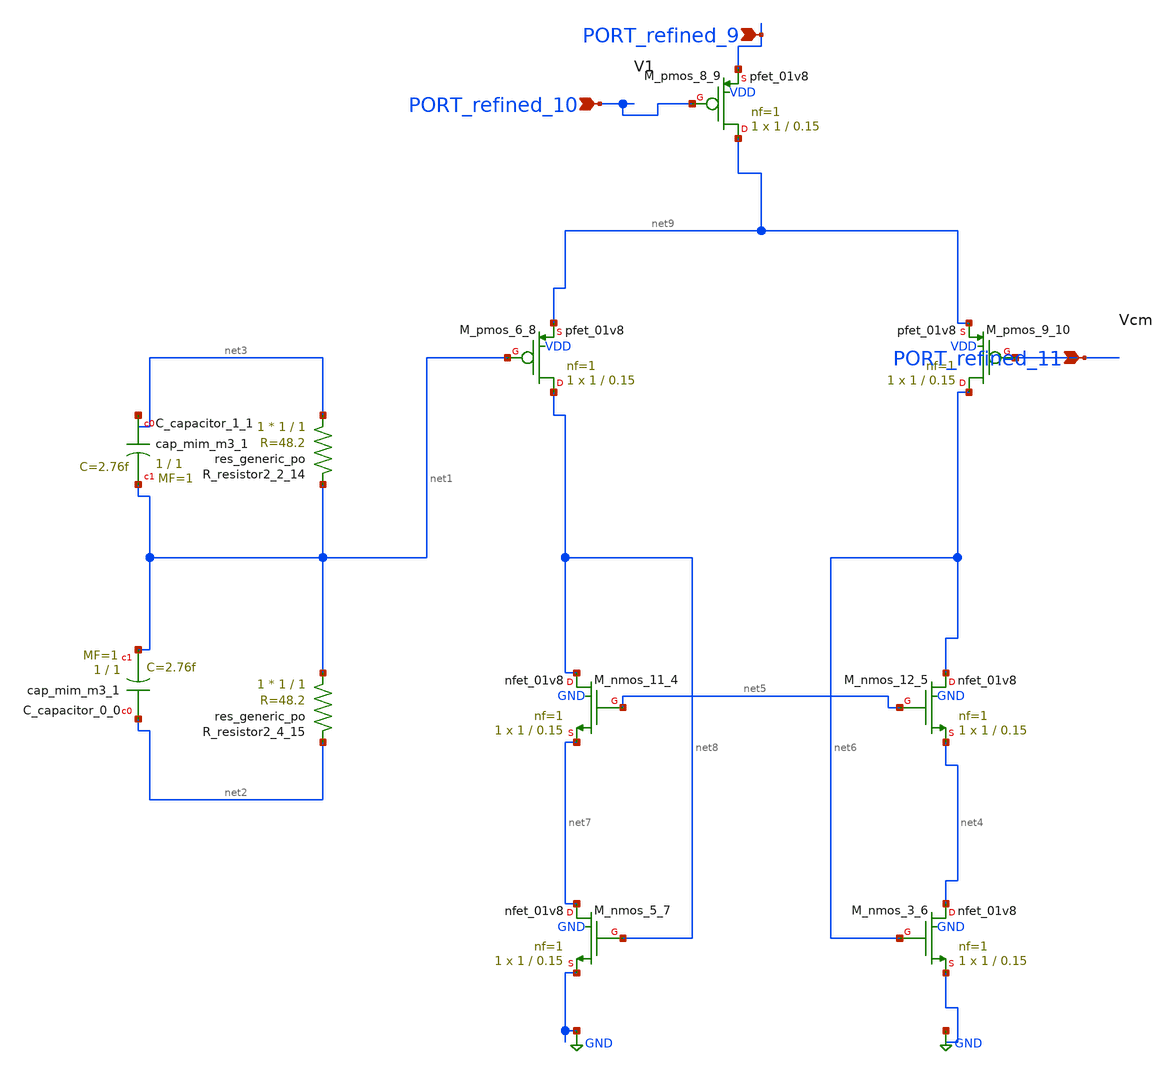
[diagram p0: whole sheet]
** sch_path: schematics/p07_fig9_cmfb.sch
**.subckt p07_fig9_cmfb PORT_refined_9 PORT_refined_10 PORT_refined_11
*.ipin PORT_refined_9
*.ipin PORT_refined_10
*.ipin PORT_refined_11
XC_capacitor_0_0 net2 net1 sky130_fd_pr__cap_mim_m3_1 W=1 L=1 MF=1 m=1
XC_capacitor_1_1 net3 net1 sky130_fd_pr__cap_mim_m3_1 W=1 L=1 MF=1 m=1
XM_nmos_11_4 net8 net5 net7 GND sky130_fd_pr__nfet_01v8 L=0.15 W=1 nf=1 ad='int((1 + 1)/2) * 1 / 1 * 0.29'
+ as='int((1 + 2)/2) * 1 / 1 * 0.29' pd='2*int((1 + 1)/2) * (1 / 1 + 0.29)' ps='2*int((1 + 2)/2) * (1 / 1 + 0.29)'
+ nrd='0.29 / 1 ' nrs='0.29 / 1 ' sa=0 sb=0 sd=0 mult=1 m=1
XM_nmos_12_5 net6 net5 net4 GND sky130_fd_pr__nfet_01v8 L=0.15 W=1 nf=1 ad='int((1 + 1)/2) * 1 / 1 * 0.29'
+ as='int((1 + 2)/2) * 1 / 1 * 0.29' pd='2*int((1 + 1)/2) * (1 / 1 + 0.29)' ps='2*int((1 + 2)/2) * (1 / 1 + 0.29)'
+ nrd='0.29 / 1 ' nrs='0.29 / 1 ' sa=0 sb=0 sd=0 mult=1 m=1
XM_nmos_3_6 net4 net6 GND GND sky130_fd_pr__nfet_01v8 L=0.15 W=1 nf=1 ad='int((1 + 1)/2) * 1 / 1 * 0.29'
+ as='int((1 + 2)/2) * 1 / 1 * 0.29' pd='2*int((1 + 1)/2) * (1 / 1 + 0.29)' ps='2*int((1 + 2)/2) * (1 / 1 + 0.29)'
+ nrd='0.29 / 1 ' nrs='0.29 / 1 ' sa=0 sb=0 sd=0 mult=1 m=1
XM_nmos_5_7 net7 net8 GND GND sky130_fd_pr__nfet_01v8 L=0.15 W=1 nf=1 ad='int((1 + 1)/2) * 1 / 1 * 0.29'
+ as='int((1 + 2)/2) * 1 / 1 * 0.29' pd='2*int((1 + 1)/2) * (1 / 1 + 0.29)' ps='2*int((1 + 2)/2) * (1 / 1 + 0.29)'
+ nrd='0.29 / 1 ' nrs='0.29 / 1 ' sa=0 sb=0 sd=0 mult=1 m=1
XM_pmos_6_8 net8 net1 net9 VDD sky130_fd_pr__pfet_01v8 L=0.15 W=1 nf=1 ad='int((1 + 1)/2) * 1 / 1 * 0.29'
+ as='int((1 + 2)/2) * 1 / 1 * 0.29' pd='2*int((1 + 1)/2) * (1 / 1 + 0.29)' ps='2*int((1 + 2)/2) * (1 / 1 + 0.29)'
+ nrd='0.29 / 1 ' nrs='0.29 / 1 ' sa=0 sb=0 sd=0 mult=1 m=1
XM_pmos_8_9 net9 PORT_refined_10 PORT_refined_9 VDD sky130_fd_pr__pfet_01v8 L=0.15 W=1 nf=1 ad='int((1 + 1)/2) * 1 / 1 * 0.29'
+ as='int((1 + 2)/2) * 1 / 1 * 0.29' pd='2*int((1 + 1)/2) * (1 / 1 + 0.29)' ps='2*int((1 + 2)/2) * (1 / 1 + 0.29)'
+ nrd='0.29 / 1 ' nrs='0.29 / 1 ' sa=0 sb=0 sd=0 mult=1 m=1
XM_pmos_9_10 net6 PORT_refined_11 net9 VDD sky130_fd_pr__pfet_01v8 L=0.15 W=1 nf=1 ad='int((1 + 1)/2) * 1 / 1 * 0.29'
+ as='int((1 + 2)/2) * 1 / 1 * 0.29' pd='2*int((1 + 1)/2) * (1 / 1 + 0.29)' ps='2*int((1 + 2)/2) * (1 / 1 + 0.29)'
+ nrd='0.29 / 1 ' nrs='0.29 / 1 ' sa=0 sb=0 sd=0 mult=1 m=1
XR_resistor2_2_14 net3 net1 sky130_fd_pr__res_generic_po W=1 L=1 m=1
XR_resistor2_4_15 net1 net2 sky130_fd_pr__res_generic_po W=1 L=1 m=1
**.ends
.GLOBAL GND
.end
